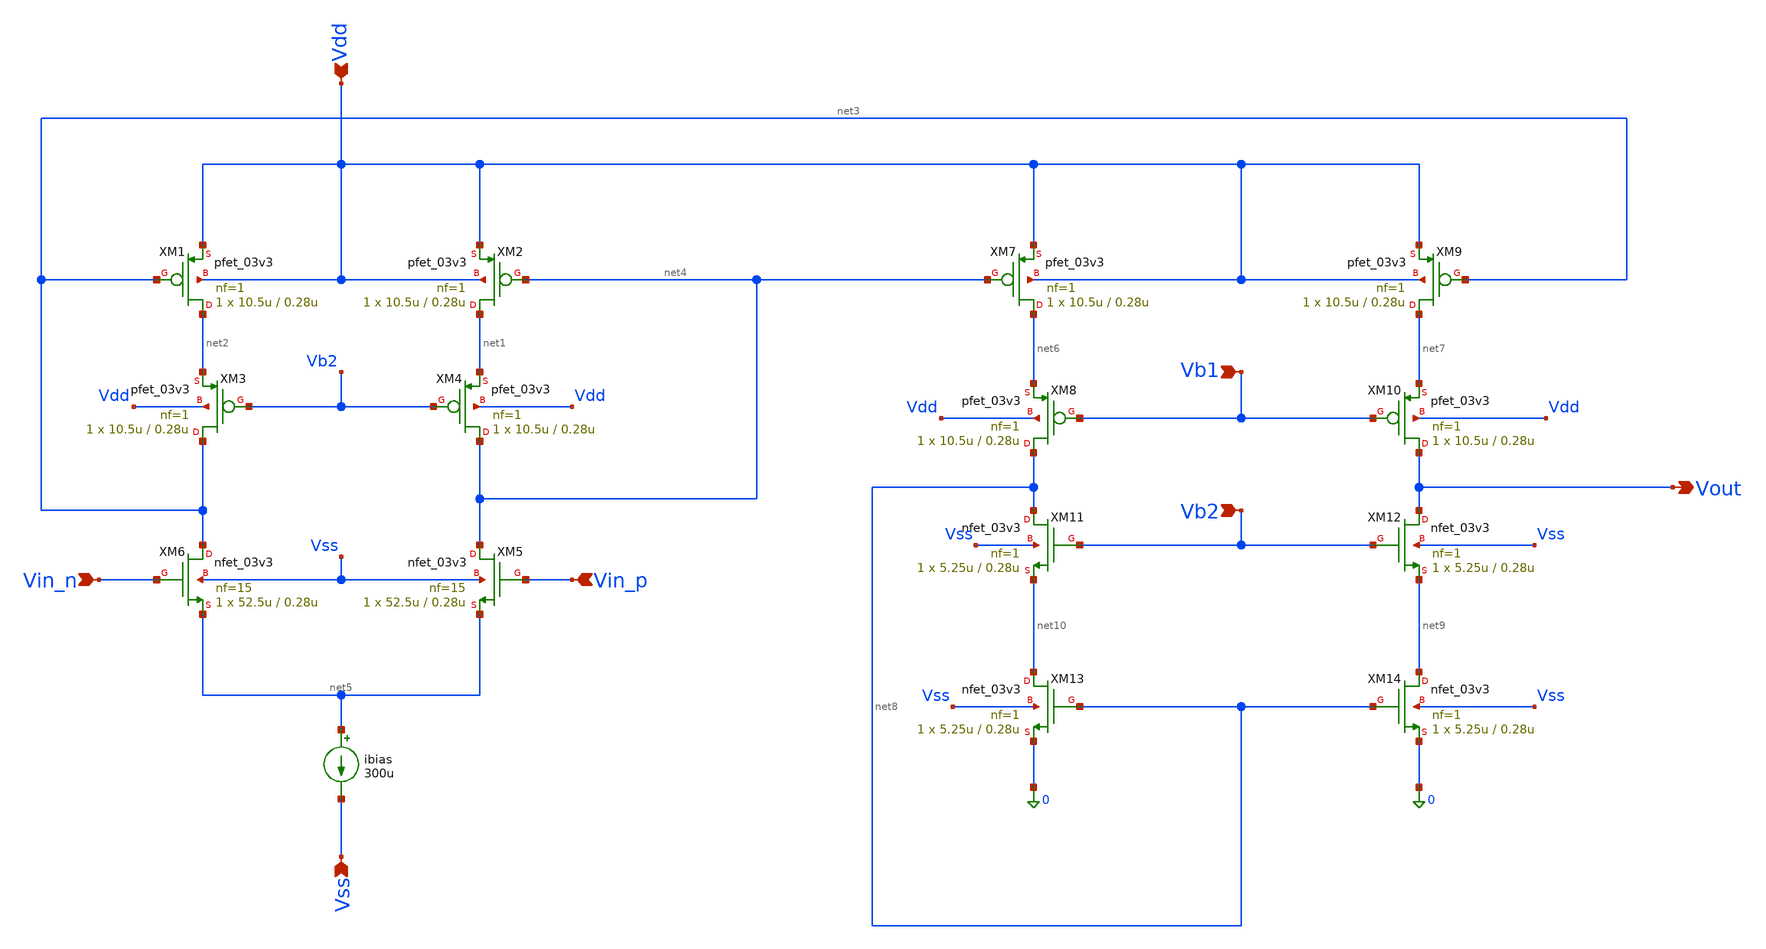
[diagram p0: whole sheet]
** sch_path: blocks/adc/lvds/op_amp.sch
**.subckt op_amp Vdd Vb2 Vin_p Vin_n Vb1 Vout Vss
*.ipin Vdd
*.ipin Vb2
*.ipin Vin_p
*.ipin Vin_n
*.ipin Vb1
*.opin Vout
*.ipin Vss
XM1 net2 net3 Vdd Vdd pfet_03v3 L=0.28u W=10.5u nf=1 ad='int((nf+1)/2) * W/nf * 0.18u' as='int((nf+2)/2) * W/nf * 0.18u'
+ pd='2*int((nf+1)/2) * (W/nf + 0.18u)' ps='2*int((nf+2)/2) * (W/nf + 0.18u)' nrd='0.18u / W' nrs='0.18u / W'
+ sa=0 sb=0 sd=0 m=1
XM2 net1 net4 Vdd Vdd pfet_03v3 L=0.28u W=10.5u nf=1 ad='int((nf+1)/2) * W/nf * 0.18u' as='int((nf+2)/2) * W/nf * 0.18u'
+ pd='2*int((nf+1)/2) * (W/nf + 0.18u)' ps='2*int((nf+2)/2) * (W/nf + 0.18u)' nrd='0.18u / W' nrs='0.18u / W'
+ sa=0 sb=0 sd=0 m=1
XM3 net3 Vb2 net2 Vdd pfet_03v3 L=0.28u W=10.5u nf=1 ad='int((nf+1)/2) * W/nf * 0.18u' as='int((nf+2)/2) * W/nf * 0.18u'
+ pd='2*int((nf+1)/2) * (W/nf + 0.18u)' ps='2*int((nf+2)/2) * (W/nf + 0.18u)' nrd='0.18u / W' nrs='0.18u / W'
+ sa=0 sb=0 sd=0 m=1
XM4 net4 Vb2 net1 Vdd pfet_03v3 L=0.28u W=10.5u nf=1 ad='int((nf+1)/2) * W/nf * 0.18u' as='int((nf+2)/2) * W/nf * 0.18u'
+ pd='2*int((nf+1)/2) * (W/nf + 0.18u)' ps='2*int((nf+2)/2) * (W/nf + 0.18u)' nrd='0.18u / W' nrs='0.18u / W'
+ sa=0 sb=0 sd=0 m=1
XM5 net4 Vin_p net5 Vss nfet_03v3 L=0.28u W=52.5u nf=15 ad='int((nf+1)/2) * W/nf * 0.18u' as='int((nf+2)/2) * W/nf * 0.18u'
+ pd='2*int((nf+1)/2) * (W/nf + 0.18u)' ps='2*int((nf+2)/2) * (W/nf + 0.18u)' nrd='0.18u / W' nrs='0.18u / W'
+ sa=0 sb=0 sd=0 m=1
XM6 net3 Vin_n net5 Vss nfet_03v3 L=0.28u W=52.5u nf=15 ad='int((nf+1)/2) * W/nf * 0.18u' as='int((nf+2)/2) * W/nf * 0.18u'
+ pd='2*int((nf+1)/2) * (W/nf + 0.18u)' ps='2*int((nf+2)/2) * (W/nf + 0.18u)' nrd='0.18u / W' nrs='0.18u / W'
+ sa=0 sb=0 sd=0 m=1
XM7 net6 net4 Vdd Vdd pfet_03v3 L=0.28u W=10.5u nf=1 ad='int((nf+1)/2) * W/nf * 0.18u' as='int((nf+2)/2) * W/nf * 0.18u'
+ pd='2*int((nf+1)/2) * (W/nf + 0.18u)' ps='2*int((nf+2)/2) * (W/nf + 0.18u)' nrd='0.18u / W' nrs='0.18u / W'
+ sa=0 sb=0 sd=0 m=1
XM9 net7 net3 Vdd Vdd pfet_03v3 L=0.28u W=10.5u nf=1 ad='int((nf+1)/2) * W/nf * 0.18u' as='int((nf+2)/2) * W/nf * 0.18u'
+ pd='2*int((nf+1)/2) * (W/nf + 0.18u)' ps='2*int((nf+2)/2) * (W/nf + 0.18u)' nrd='0.18u / W' nrs='0.18u / W'
+ sa=0 sb=0 sd=0 m=1
XM11 net8 Vb2 net10 Vss nfet_03v3 L=0.28u W=5.25u nf=1 ad='int((nf+1)/2) * W/nf * 0.18u' as='int((nf+2)/2) * W/nf * 0.18u'
+ pd='2*int((nf+1)/2) * (W/nf + 0.18u)' ps='2*int((nf+2)/2) * (W/nf + 0.18u)' nrd='0.18u / W' nrs='0.18u / W'
+ sa=0 sb=0 sd=0 m=1
XM12 Vout Vb2 net9 Vss nfet_03v3 L=0.28u W=5.25u nf=1 ad='int((nf+1)/2) * W/nf * 0.18u' as='int((nf+2)/2) * W/nf * 0.18u'
+ pd='2*int((nf+1)/2) * (W/nf + 0.18u)' ps='2*int((nf+2)/2) * (W/nf + 0.18u)' nrd='0.18u / W' nrs='0.18u / W'
+ sa=0 sb=0 sd=0 m=1
XM13 net10 net8 0 Vss nfet_03v3 L=0.28u W=5.25u nf=1 ad='int((nf+1)/2) * W/nf * 0.18u' as='int((nf+2)/2) * W/nf * 0.18u'
+ pd='2*int((nf+1)/2) * (W/nf + 0.18u)' ps='2*int((nf+2)/2) * (W/nf + 0.18u)' nrd='0.18u / W' nrs='0.18u / W'
+ sa=0 sb=0 sd=0 m=1
XM14 net9 net8 0 Vss nfet_03v3 L=0.28u W=5.25u nf=1 ad='int((nf+1)/2) * W/nf * 0.18u' as='int((nf+2)/2) * W/nf * 0.18u'
+ pd='2*int((nf+1)/2) * (W/nf + 0.18u)' ps='2*int((nf+2)/2) * (W/nf + 0.18u)' nrd='0.18u / W' nrs='0.18u / W'
+ sa=0 sb=0 sd=0 m=1
XM8 net8 Vb1 net6 Vdd pfet_03v3 L=0.28u W=10.5u nf=1 ad='int((nf+1)/2) * W/nf * 0.18u' as='int((nf+2)/2) * W/nf * 0.18u'
+ pd='2*int((nf+1)/2) * (W/nf + 0.18u)' ps='2*int((nf+2)/2) * (W/nf + 0.18u)' nrd='0.18u / W' nrs='0.18u / W'
+ sa=0 sb=0 sd=0 m=1
XM10 Vout Vb1 net7 Vdd pfet_03v3 L=0.28u W=10.5u nf=1 ad='int((nf+1)/2) * W/nf * 0.18u' as='int((nf+2)/2) * W/nf * 0.18u'
+ pd='2*int((nf+1)/2) * (W/nf + 0.18u)' ps='2*int((nf+2)/2) * (W/nf + 0.18u)' nrd='0.18u / W' nrs='0.18u / W'
+ sa=0 sb=0 sd=0 m=1
ibias net5 Vss 300u
**.ends
.end
